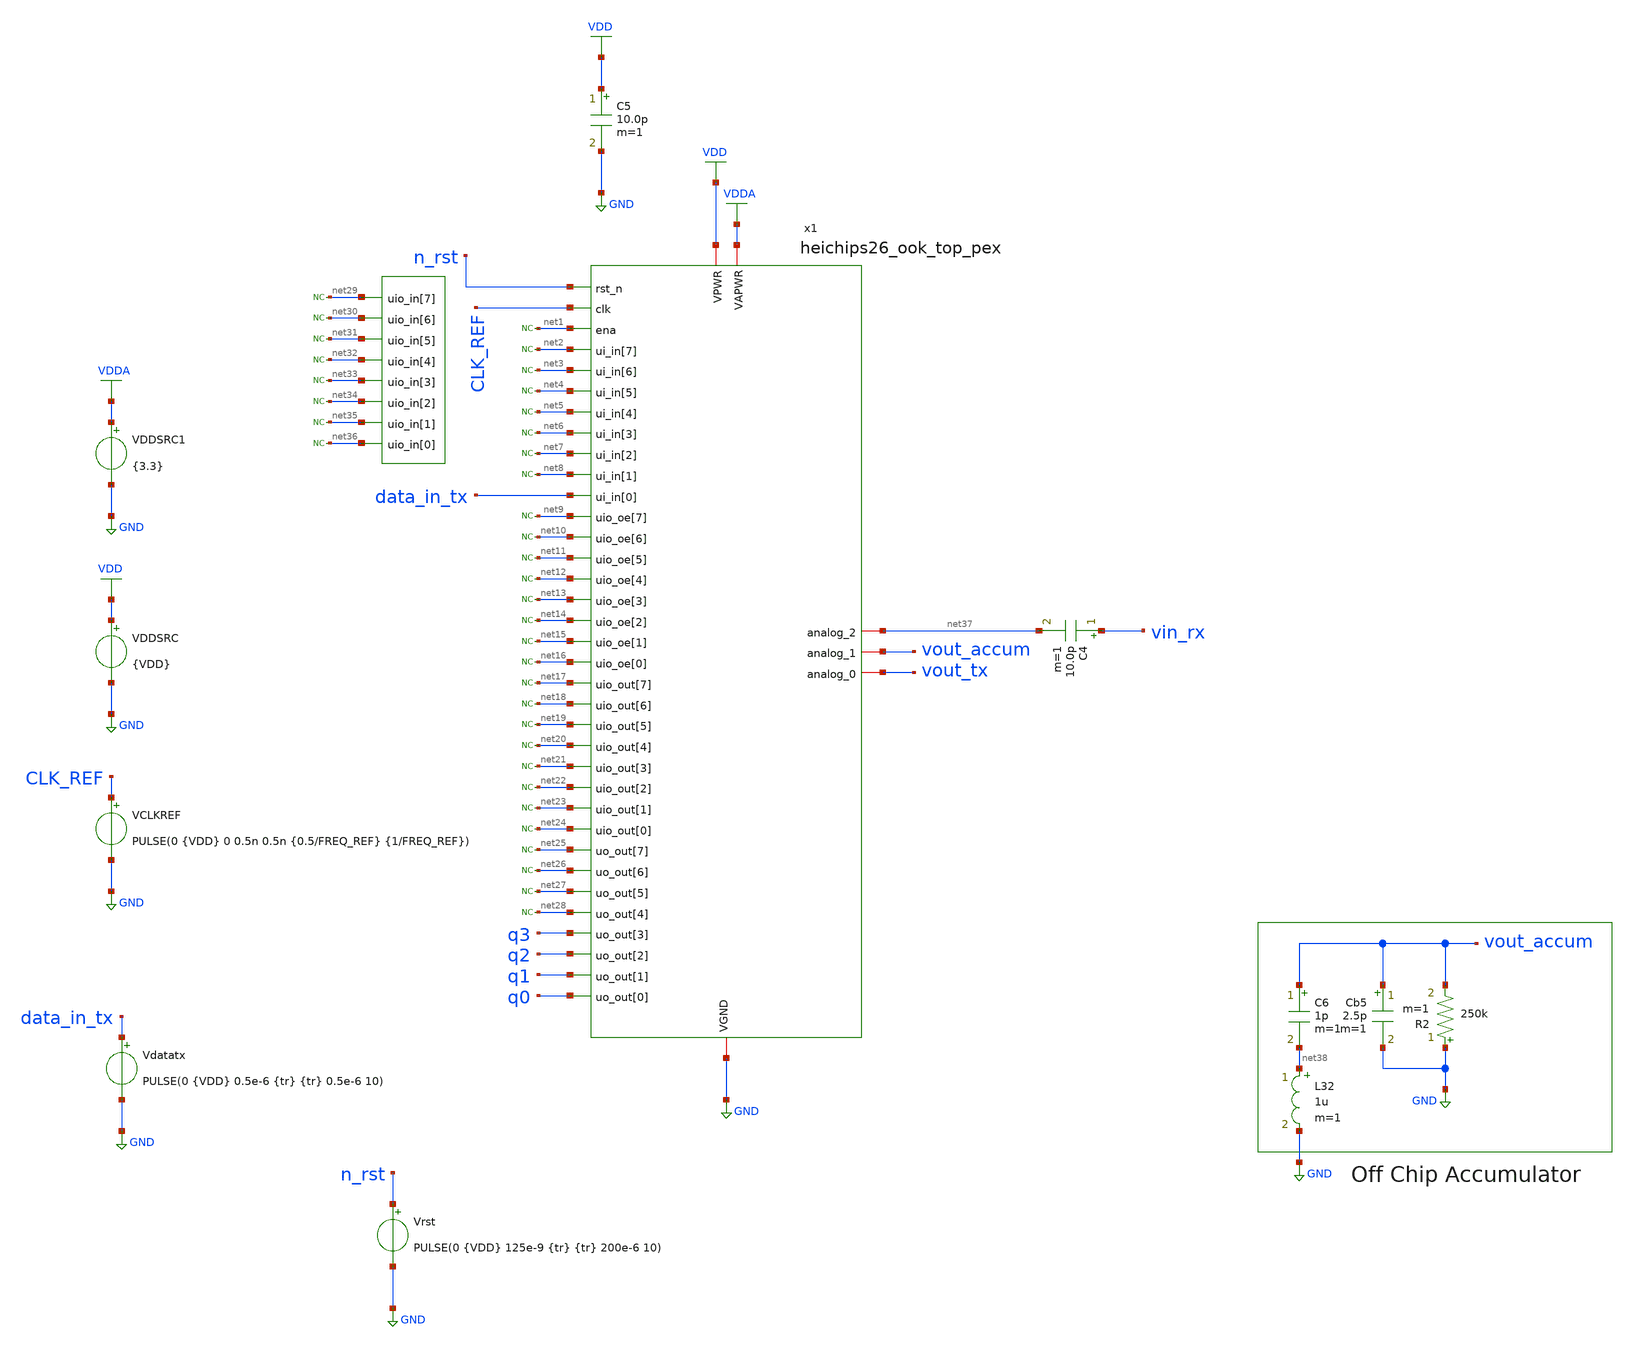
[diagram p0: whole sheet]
** sch_path: macros/heichips26_ook_top/testbenches/xschem/heichipts26_ook_top_tb_tran.sch
**.subckt heichipts26_ook_top_tb_tran
VCLKREF CLK_REF GND PULSE(0 {VDD} 0 0.5n 0.5n {0.5/FREQ_REF} {1/FREQ_REF})
VDDSRC VDD GND {VDD}
VDDSRC1 VDDA GND {3.3}
Cb5 vout_accum GND 2.5p m=1
R2 GND vout_accum 250k m=1
* noconn #net28
* noconn #net27
* noconn #net26
* noconn #net25
* noconn #net24
* noconn #net23
* noconn #net22
* noconn #net21
* noconn #net20
* noconn #net19
* noconn #net18
* noconn #net17
* noconn #net16
* noconn #net15
* noconn #net14
* noconn #net13
* noconn #net12
* noconn #net11
* noconn #net10
* noconn #net9
* noconn #net8
* noconn #net7
* noconn #net6
* noconn #net5
* noconn #net4
* noconn #net3
* noconn #net2
* noconn #net1
Vrst n_rst GND PULSE(0 {VDD} 125e-9 {tr} {tr} 200e-6 10)
Vdatatx data_in_tx GND PULSE(0 {VDD} 0.5e-6 {tr} {tr} 0.5e-6 10)
* noconn #net36
* noconn #net35
* noconn #net34
* noconn #net33
* noconn #net32
* noconn #net31
* noconn #net30
* noconn #net29
x1 net1 net19 net9 net2 net10 net20 net3 net21 net11 net22 net12 net4 net5 net13 net23 net24 net14
+ net6 VDD VDDA net7 net15 net25 net37 vout_accum vout_tx q3 q2 q1 q0 net8 net26 net16 n_rst CLK_REF
+ data_in_tx net27 net17 GND net18 net28 net29 net30 net31 net32 net33 net34 net35 net36 heichips26_ook_top_pex
C4 vin_rx net37 10.0p m=1
C5 VDD GND 10.0p m=1
C6 vout_accum net38 1p m=1
L32 net38 GND 1u m=1
**** begin user architecture code


.param VDD=1.5
.param FREQ_REF=80e6
.param tr=1e-9
.param tr_data=50e-9
.options klu reltol=1e-3 abstol=1e-12 vntol=1e-6 gmin=1e-12 itl1=200 itl4=100 rshunt=1e9 trtol=20
.param b0=1 b1=0 b2=1 b3=0 b4=0 b5=1 b6=0 b7=1
.param bitsum={b0+b1+b2+b3+b4+b5+b6+b7}
.param parity={bitsum-2*int(bitsum/2)}

* Stepped voltage ladder (amplitude, in volts): ~0/1mV/5mV/10mV, 0.1us each,
* then held at 10mV through the rest of the (unchanged) .tran span
Venv nenv 0 PWL(  0 1e-12                     {0.1e-6-tr} 1e-12  0.1e-6 1m                   {0.2e-6-tr}
+ 1m  0.2e-6 5m                   {0.3e-6-tr} 5m  0.3e-6 10m                  {1.5e-6-tr} 10m  1.5e-6 0
+                    150e-6 0 )

* Carrier folded into one B-source (one less node); nenv now carries the
* step amplitude directly in volts, no separate 1e-3 scale factor needed
Bvin1 vin_rx 0 V={(V(nenv)*sin(6.283185307*433.92e6*time))}

.save vout_accum vin_rx rx_filt i(VDDSRC) i(VDDSRC1)
.save x1.heichips26_ook_soc_0.q0 x1.heichips26_ook_soc_0.q1 x1.heichips26_ook_soc_0.q2 x1.heichips26_ook_soc_0.q3
.save q0 q1 q2 q3
.save x1.heichips26_ook_soc_0.q0_int x1.heichips26_ook_soc_0.q0_diff
.save x1.heichips26_ook_soc_0.amp_s3_cap1 x1.heichips26_ook_soc_0.amp_s3_cap2
.save x1.heichips26_ook_soc_0.vref1 x1.heichips26_ook_soc_0.vref2 x1.heichips26_ook_soc_0.vref3 x1.heichips26_ook_soc_0.vref4
.save x1.heichips26_ook_soc_0.clk_fb x1.heichips26_ook_soc_0.vctrl_in x1.heichips26_ook_soc_0.vctrl_b_in
.save data_in_tx
.save x1.heichips26_ook_soc_0.vcl
.save vout_accum
.tran 100p 150u 0 100p



.lib cornerMOSlv.lib mos_tt
.lib cornerMOShv.lib mos_tt
.lib cornerRES.lib res_typ
.lib cornerDIO.lib dio_tt
.lib cornerCAP.lib cap_typ
.include /home/belal/HeiChips/heichips26-on-off/macros/heichips26_ook_top/macros/dac/netlist/xspice/dac.xspice
.include /home/belal/HeiChips/heichips26-on-off/macros/heichips26_ook_top/macros/ook_analog_system/netlist/pex/ook_transmitter_magic_pex_3.spice
.include /home/belal/HeiChips/heichips26-on-off/macros/heichips26_ook_top/macros/ook_analog_system/netlist/pex/ook_analog_system_magic_pex_3.spice
.include /home/belal/HeiChips/heichips26-on-off/IHP-Open-PDK/ihp-sg13cmos5l/libs.tech/ngspice/models/cap_mfringe.lib
.include /home/belal/HeiChips/heichips26-on-off/macros/heichips26_ook_top/macros/ook_analog_system/netlist/pex/vco_magic_pex_3.spice
.include /home/belal/HeiChips/heichips26-on-off/macros/heichips26_ook_top/macros/ook_analog_system/netlist/pex/output_buffer_magic_pex_3.spice
.include /home/belal/HeiChips/heichips26-on-off/macros/heichips26_ook_top/netlist/pex/heichips26_ook_top_magic_pex_3.spice
.include /home/belal/HeiChips/heichips26-on-off/IHP-Open-PDK/ihp-sg13cmos5l/libs.ref/sg13cmos5l_io/spice/sg13cmos5l_io.spi

**** end user architecture code
**.ends
.GLOBAL GND
.GLOBAL VDD
.GLOBAL VDDA
.end
